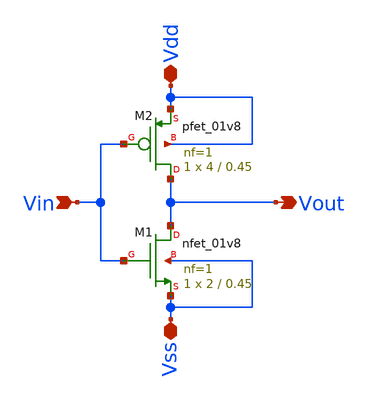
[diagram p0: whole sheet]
** sch_path: Current Starved VCO for PLL/xschem/inverter.sch
**.subckt inverter Vdd Vout Vss Vin
*.iopin Vdd
*.opin Vout
*.iopin Vss
*.ipin Vin
XM1 Vout Vin Vss Vss sky130_fd_pr__nfet_01v8 L=0.45 W=2 nf=1 ad='int((nf+1)/2) * W/nf * 0.29' as='int((nf+2)/2) * W/nf * 0.29'
+ pd='2*int((nf+1)/2) * (W/nf + 0.29)' ps='2*int((nf+2)/2) * (W/nf + 0.29)' nrd='0.29 / W' nrs='0.29 / W'
+ sa=0 sb=0 sd=0 mult=1 m=1
XM2 Vout Vin Vdd Vdd sky130_fd_pr__pfet_01v8 L=0.45 W=4 nf=1 ad='int((nf+1)/2) * W/nf * 0.29' as='int((nf+2)/2) * W/nf * 0.29'
+ pd='2*int((nf+1)/2) * (W/nf + 0.29)' ps='2*int((nf+2)/2) * (W/nf + 0.29)' nrd='0.29 / W' nrs='0.29 / W'
+ sa=0 sb=0 sd=0 mult=1 m=1
**.ends
.end
